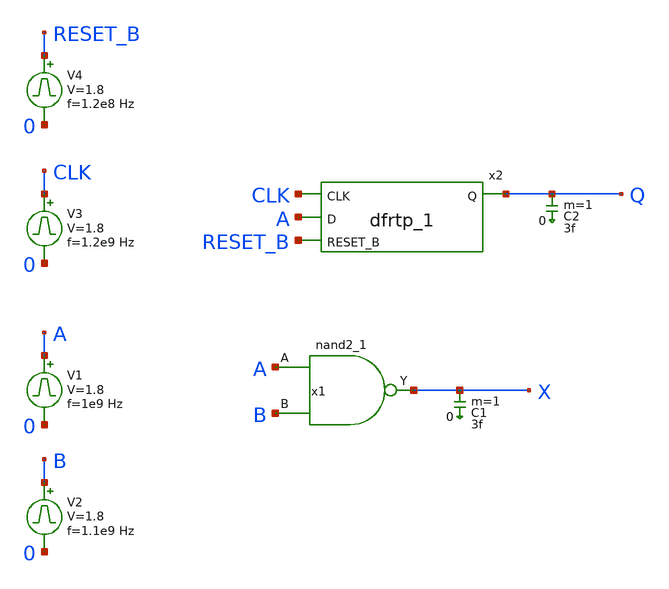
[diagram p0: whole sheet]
** sch_path: sky130_tests/test_stdcells.sch
* Copyright 2020 Stefan Frederik Schippers
* Licensed under the Apache License, Version 2.0 (the "License");
* you may not use this file except in compliance with the License.
* You may obtain a copy of the License at
* https://www.apache.org/licenses/LICENSE-2.0
* Unless required by applicable law or agreed to in writing, software
* distributed under the License is distributed on an "AS IS" BASIS,
* WITHOUT WARRANTIES OR CONDITIONS OF ANY KIND, either express or implied.
* See the License for the specific language governing permissions and
* limitations under the License.
**.subckt test_stdcells
x1 A B VSS VSS VCC VCC X sky130_fd_sc_hd__nand2_1
V1 A 0 pulse 0 1.8 '0.495/ 1e9 ' '0.01/1e9 ' '0.01/1e9 ' '0.49/1e9 ' '1/1e9 '
V2 B 0 pulse 0 1.8 '0.495/ 1.1e9 ' '0.01/1.1e9 ' '0.01/1.1e9 ' '0.49/1.1e9 ' '1/1.1e9 '
C1 X 0 3f m=1
x2 CLK A RESET_B VSS VSS VCC VCC Q sky130_fd_sc_hd__dfrtp_1
V3 CLK 0 pulse 0 1.8 '0.495/ 1.2e9 ' '0.01/1.2e9 ' '0.01/1.2e9 ' '0.49/1.2e9 ' '1/1.2e9 '
V4 RESET_B 0 pulse 0 1.8 '0.495/ 1.2e8 ' '0.01/1.2e8 ' '0.01/1.2e8 ' '0.49/1.2e8 ' '1/1.2e8 '
C2 Q 0 3f m=1
**.ends
**** begin user architecture code
eval(* .option SCALE=1e-6
.temp 25

* .include /home/schippes/skywater-pdk/sky130_fd_sc_hd/cells/nand2/sky130_fd_sc_hd__nand2_1.spice
* .include /home/schippes/skywater-pdk/sky130_fd_sc_hd/cells/dfrtp/sky130_fd_sc_hd__dfrtp_1.spice
.include $SKYWATER_STDCELLS\/cells/nand2/sky130_fd_sc_hd__nand2_1.spice
.include $SKYWATER_STDCELLS\/cells/dfrtp/sky130_fd_sc_hd__dfrtp_1.spice
**
vvcc vcc 0 dc 1.8
vvss vss 0 0
.tran 10p 80n
 )

.include   ~/skywater-pdk/sky130_fd_pr_ngspice/cells/nfet_01v8/sky130_fd_pr__nfet_01v8__tt.corner.spice
.include ~/skywater-pdk/sky130_fd_pr_ngspice/cells/nfet_01v8_lvt/sky130_fd_pr__nfet_01v8_lvt__tt.corner.spice
.include ~/skywater-pdk/sky130_fd_pr_ngspice/cells/pfet_01v8/sky130_fd_pr__pfet_01v8__tt.corner.spice
.include ~/skywater-pdk/sky130_fd_pr_ngspice/cells/nfet_03v3_nvt/sky130_fd_pr__nfet_03v3_nvt__tt.corner.spice
.include ~/skywater-pdk/sky130_fd_pr_ngspice/cells/nfet_05v0_nvt/sky130_fd_pr__nfet_05v0_nvt__tt.corner.spice
.include ~/skywater-pdk/sky130_fd_pr_ngspice/cells/esd_nfet_01v8/sky130_fd_pr__esd_nfet_01v8__tt.corner.spice
.include ~/skywater-pdk/sky130_fd_pr_ngspice/cells/pfet_01v8_lvt/sky130_fd_pr__pfet_01v8_lvt__tt.corner.spice
.include ~/skywater-pdk/sky130_fd_pr_ngspice/cells/pfet_01v8_hvt/sky130_fd_pr__pfet_01v8_hvt__tt.corner.spice
.include ~/skywater-pdk/sky130_fd_pr_ngspice/cells/esd_pfet_g5v0d10v5/sky130_fd_pr__esd_pfet_g5v0d10v5__tt.corner.spice
.include ~/skywater-pdk/sky130_fd_pr_ngspice/cells/pfet_g5v0d10v5/sky130_fd_pr__pfet_g5v0d10v5__tt.corner.spice
.include ~/skywater-pdk/sky130_fd_pr_ngspice/cells/pfet_g5v0d16v0/sky130_fd_pr__pfet_g5v0d16v0__tt.corner.spice
.include ~/skywater-pdk/sky130_fd_pr_ngspice/cells/nfet_g5v0d10v5/sky130_fd_pr__nfet_g5v0d10v5__tt.corner.spice
.include ~/skywater-pdk/sky130_fd_pr_ngspice/cells/nfet_g5v0d16v0/sky130_fd_pr__nfet_g5v0d16v0__tt_discrete.corner.spice
.include ~/skywater-pdk/sky130_fd_pr_ngspice/cells/esd_nfet_g5v0d10v5/sky130_fd_pr__esd_nfet_g5v0d10v5__tt.corner.spice
.include ~/skywater-pdk/sky130_fd_pr_ngspice/models/corners/tt/nonfet.spice
* Mismatch parameters
.include ~/skywater-pdk/sky130_fd_pr_ngspice/cells/nfet_01v8/sky130_fd_pr__nfet_01v8__mismatch.corner.spice
.include ~/skywater-pdk/sky130_fd_pr_ngspice/cells/pfet_01v8/sky130_fd_pr__pfet_01v8__mismatch.corner.spice
.include ~/skywater-pdk/sky130_fd_pr_ngspice/cells/nfet_01v8_lvt/sky130_fd_pr__nfet_01v8_lvt__mismatch.corner.spice
.include ~/skywater-pdk/sky130_fd_pr_ngspice/cells/pfet_01v8_lvt/sky130_fd_pr__pfet_01v8_lvt__mismatch.corner.spice
.include ~/skywater-pdk/sky130_fd_pr_ngspice/cells/pfet_01v8_hvt/sky130_fd_pr__pfet_01v8_hvt__mismatch.corner.spice
.include ~/skywater-pdk/sky130_fd_pr_ngspice/cells/nfet_g5v0d10v5/sky130_fd_pr__nfet_g5v0d10v5__mismatch.corner.spice
.include ~/skywater-pdk/sky130_fd_pr_ngspice/cells/pfet_g5v0d10v5/sky130_fd_pr__pfet_g5v0d10v5__mismatch.corner.spice
.include ~/skywater-pdk/sky130_fd_pr_ngspice/cells/nfet_05v0_nvt/sky130_fd_pr__nfet_05v0_nvt__mismatch.corner.spice
.include ~/skywater-pdk/sky130_fd_pr_ngspice/cells/nfet_03v3_nvt/sky130_fd_pr__nfet_03v3_nvt__mismatch.corner.spice
* Resistor/Capacitor
.include ~/skywater-pdk/sky130_fd_pr_ngspice/models/r+c/res_typical__cap_typical.spice
.include ~/skywater-pdk/sky130_fd_pr_ngspice/models/r+c/res_typical__cap_typical__lin.spice
* Special cells
.include ~/skywater-pdk/sky130_fd_pr_ngspice/models/corners/tt/specialized_cells.spice
* All models
.include ~/skywater-pdk/sky130_fd_pr_ngspice/models/all.spice
* Corner
.include ~/skywater-pdk/sky130_fd_pr_ngspice/models/corners/tt/rf.spice


**** end user architecture code
.end
